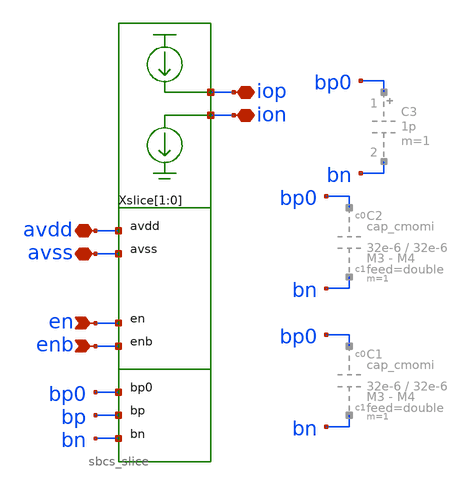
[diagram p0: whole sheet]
** sch_path: macros/sbcs/schematic/xschem/sbcs.sch
**.subckt sbcs avdd avss iop ion en enb
*.iopin avdd
*.iopin avss
*.iopin iop
*.iopin ion
*.ipin en
*.ipin enb
Xslice[1] iop ion avdd avss en enb bp0 bp bn sbcs_slice
Xslice[0] iop ion avdd avss en enb bp0 bp bn sbcs_slice
**.ends
.end
